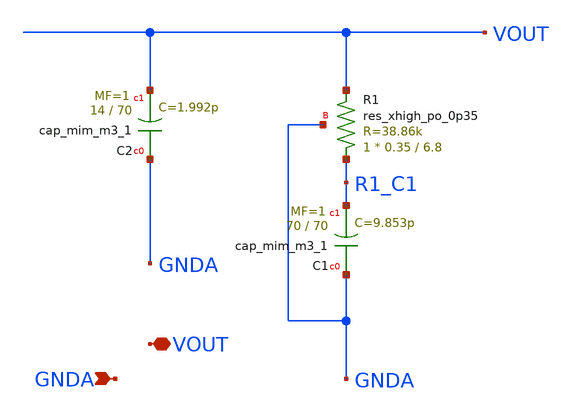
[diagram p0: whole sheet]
** sch_path: projects/pll/charge_pump/xschem_ngspice/loop_filter_xschem_2.sch
**.subckt loop_filter_xschem_2 GNDA VOUT
*.ipin GNDA
*.iopin VOUT
XC2 GNDA VOUT sky130_fd_pr__cap_mim_m3_1 W=14 L=70 MF=1 m=1
XC1 GNDA R1_C1 sky130_fd_pr__cap_mim_m3_1 W=70 L=70 MF=1 m=1
XR1 R1_C1 VOUT GNDA sky130_fd_pr__res_xhigh_po_0p35 L=6.8 mult=1 m=1
**.ends
.end
